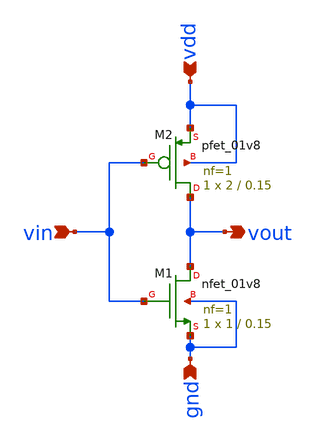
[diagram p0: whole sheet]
** sch_path: Projects/Schematic_Design_and_Analysis_of_an_8-Word_8-Bit_Static_RAM_with_6T_Storage_Cells_using_SKY130PDK/assets/schematic/inverter.sch
**.subckt inverter vin vdd gnd vout
*.ipin vin
*.ipin vdd
*.ipin gnd
*.opin vout
XM1 vout vin gnd gnd sky130_fd_pr__nfet_01v8 L=0.15 W=1 nf=1 ad='int((nf+1)/2) * W/nf * 0.29' as='int((nf+2)/2) * W/nf * 0.29'
+ pd='2*int((nf+1)/2) * (W/nf + 0.29)' ps='2*int((nf+2)/2) * (W/nf + 0.29)' nrd='0.29 / W' nrs='0.29 / W'
+ sa=0 sb=0 sd=0 mult=1 m=1
XM2 vout vin vdd vdd sky130_fd_pr__pfet_01v8 L=0.15 W=2 nf=1 ad='int((nf+1)/2) * W/nf * 0.29' as='int((nf+2)/2) * W/nf * 0.29'
+ pd='2*int((nf+1)/2) * (W/nf + 0.29)' ps='2*int((nf+2)/2) * (W/nf + 0.29)' nrd='0.29 / W' nrs='0.29 / W'
+ sa=0 sb=0 sd=0 mult=1 m=1
**.ends
.end
